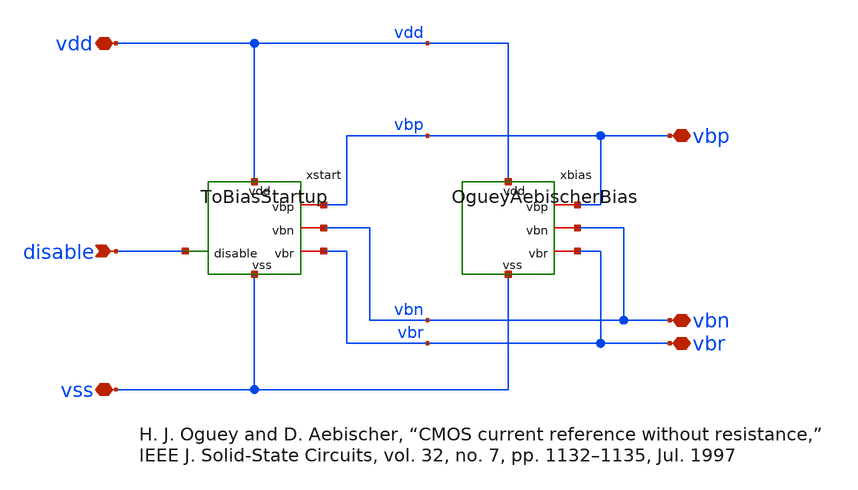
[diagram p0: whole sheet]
** sch_path: xschem/reference.sch
**.subckt reference vss vdd vbp vbn vbr disable
*.iopin vss
*.iopin vdd
*.iopin vbp
*.iopin vbn
*.iopin vbr
*.ipin disable
xbias vdd vbp vbn vbr vss OgueyAebischerBias
xstart vdd vbp vbn disable vbr vss ToBiasStartup
**.ends
.end
